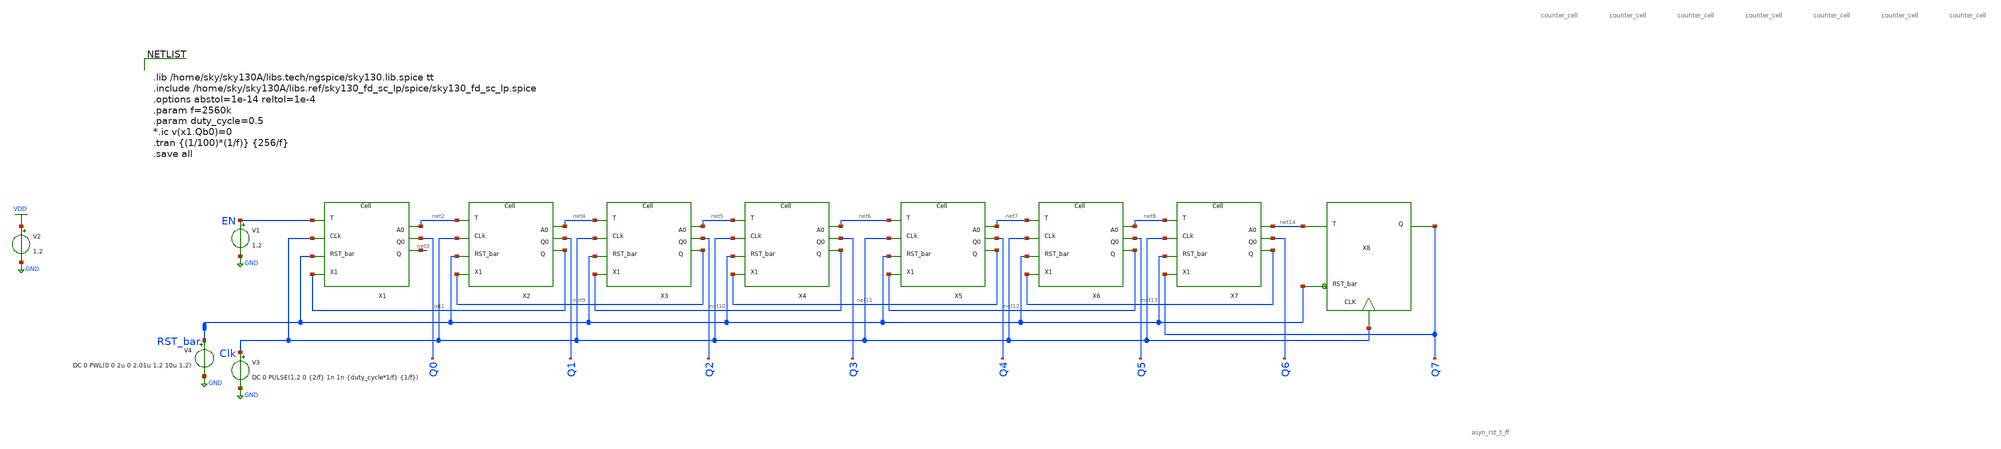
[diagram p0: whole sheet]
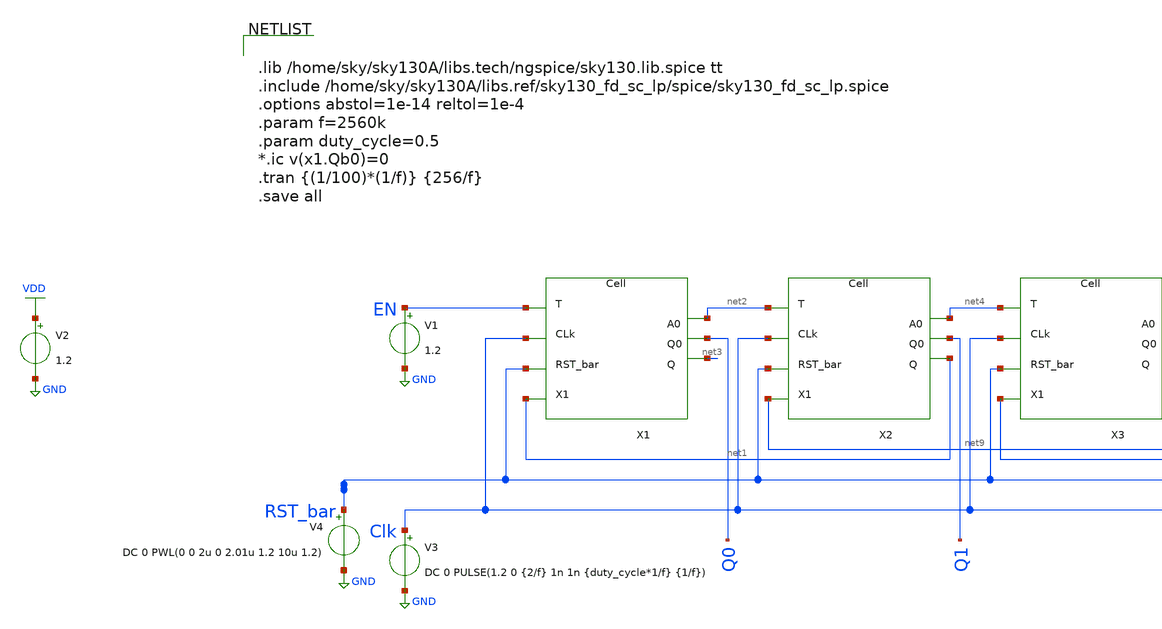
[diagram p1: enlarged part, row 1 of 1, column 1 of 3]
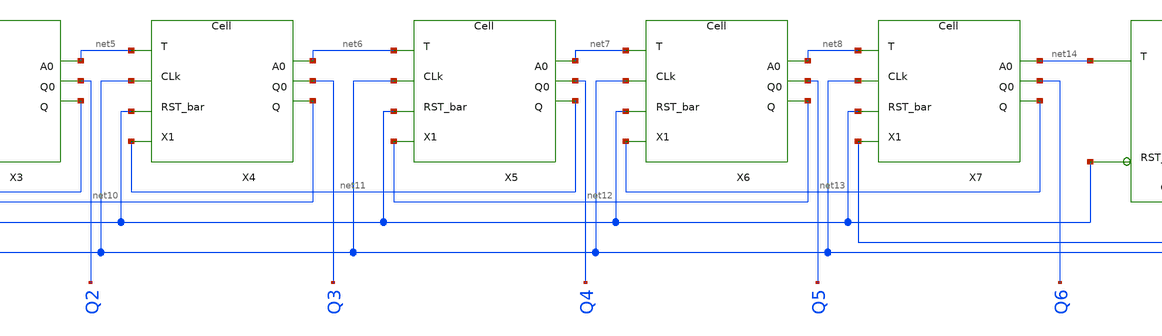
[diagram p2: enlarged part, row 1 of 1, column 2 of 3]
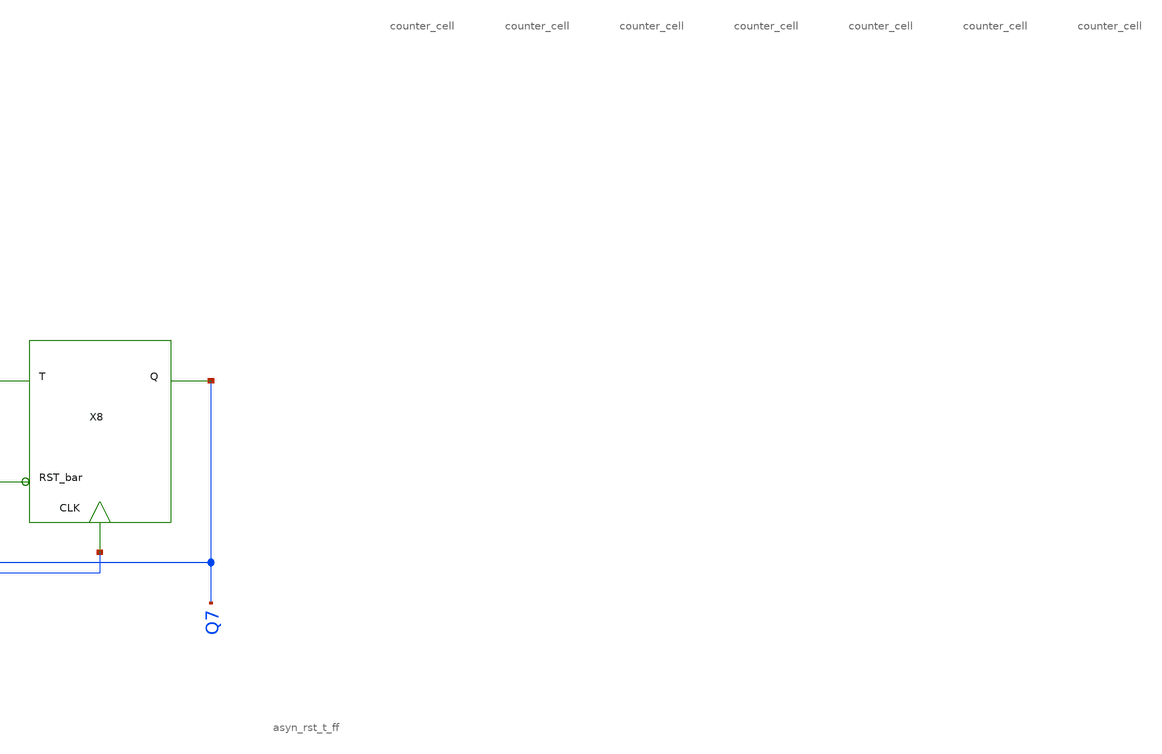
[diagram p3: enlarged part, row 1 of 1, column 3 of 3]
** sch_path: xschem/Asyn_rst_gray_counter/counter_8bit_tb.sch
**.subckt counter_8bit_tb
V3 Clk GND DC 0 PULSE(1.2 0 {2/f} 1n 1n {duty_cycle*1/f} {1/f})
V1 EN GND 1.2
V2 VDD GND 1.2
V4 RST_bar GND DC 0 PWL(0 0 2u 0 2.01u 1.2 10u 1.2)
X1 net1 RST_bar Clk EN net2 net3 Q0 counter_cell
X2 net9 RST_bar Clk net2 net4 net1 Q1 counter_cell
X3 net10 RST_bar Clk net4 net5 net9 Q2 counter_cell
X4 net11 RST_bar Clk net5 net6 net10 Q3 counter_cell
X5 net12 RST_bar Clk net6 net7 net11 Q4 counter_cell
X6 net13 RST_bar Clk net7 net8 net12 Q5 counter_cell
X7 Q7 RST_bar Clk net8 net14 net13 Q6 counter_cell
X8 net14 Q7 Clk RST_bar asyn_rst_t_ff
**** begin user architecture code


.lib /home/sky/sky130A/libs.tech/ngspice/sky130.lib.spice tt
.include /home/sky/sky130A/libs.ref/sky130_fd_sc_lp/spice/sky130_fd_sc_lp.spice
.options abstol=1e-14 reltol=1e-4
.param f=2560k
.param duty_cycle=0.5
*.ic v(x1.Qb0)=0
.tran {(1/100)*(1/f)} {256/f}
.save all


**** end user architecture code
**.ends
.GLOBAL GND
.GLOBAL VDD
.end
